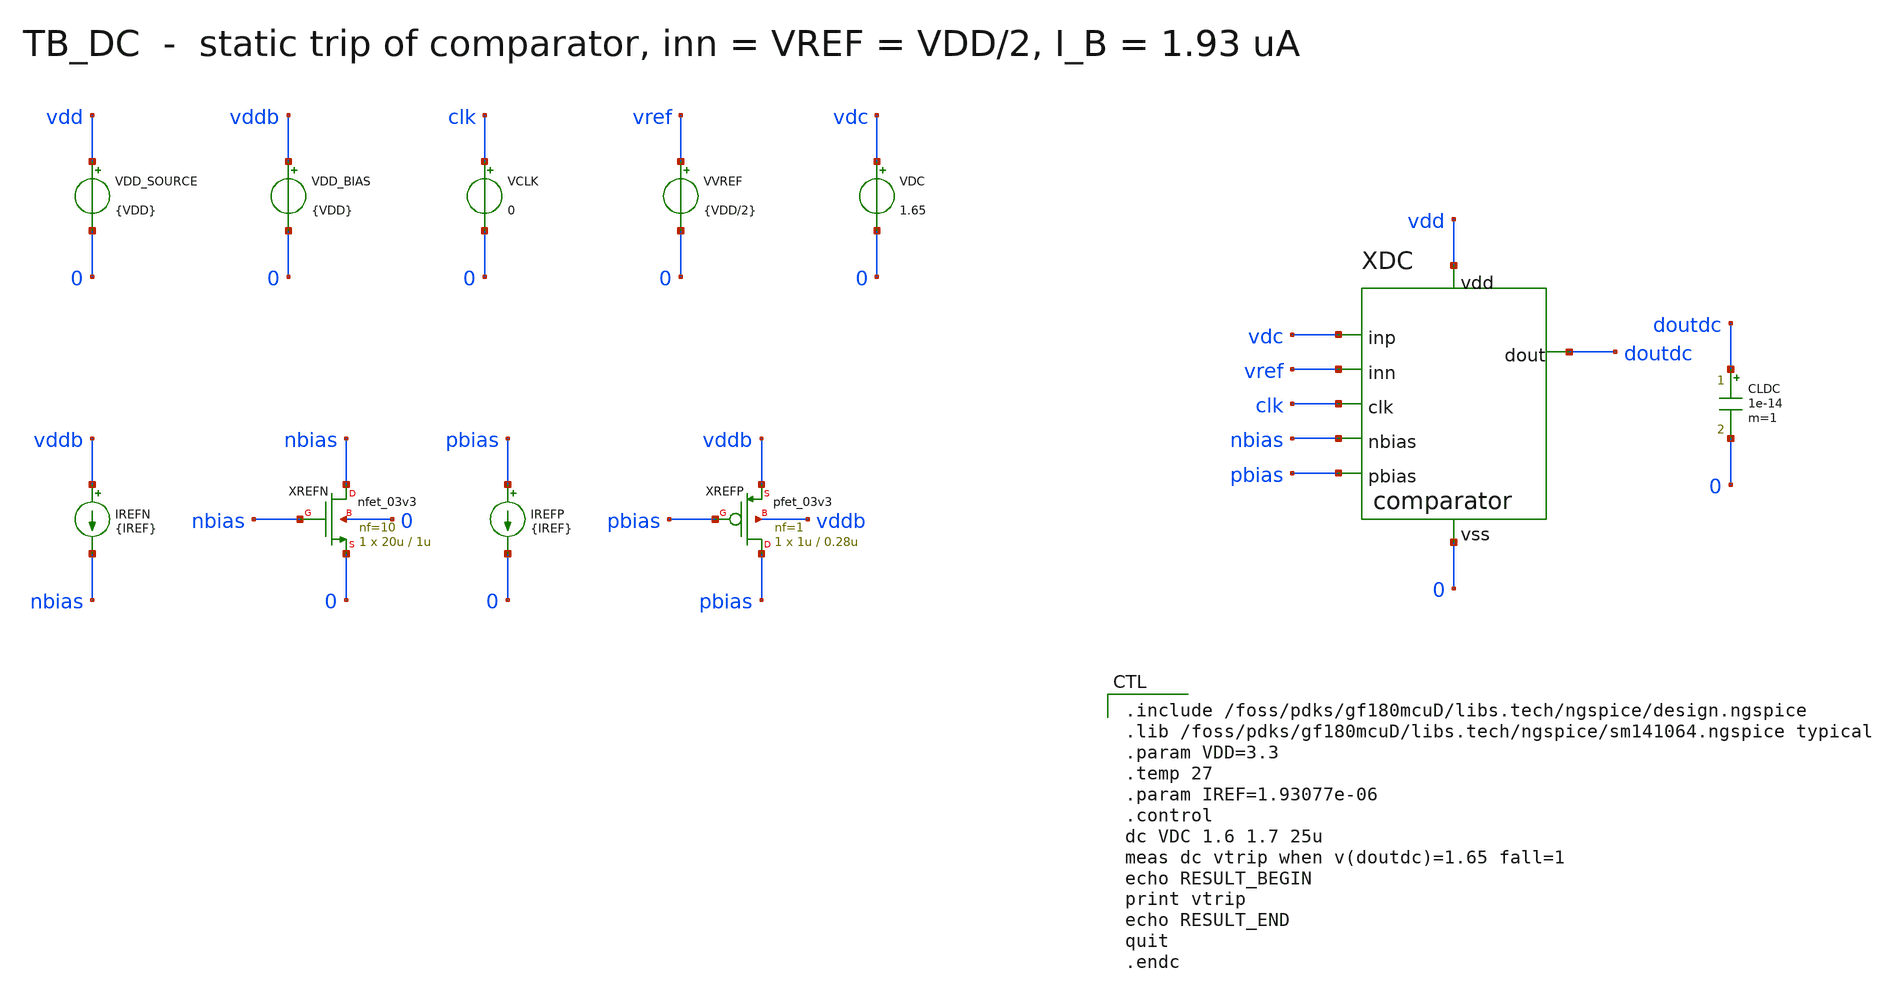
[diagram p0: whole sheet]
** sch_path: mixed_signal/comparator/tb_dc.sch
**.subckt tb_dc
VDD_SOURCE vdd 0 {VDD}
VDD_BIAS vddb 0 {VDD}
IREFN vddb nbias {IREF}
XREFN nbias nbias 0 0 nfet_03v3 L=1u W=20u nf=10 ad='int((nf+1)/2) * W/nf * 0.18u' as='int((nf+2)/2) * W/nf * 0.18u'
+ pd='2*int((nf+1)/2) * (W/nf + 0.18u)' ps='2*int((nf+2)/2) * (W/nf + 0.18u)' nrd='0.18u / W' nrs='0.18u / W'
+ sa=0 sb=0 sd=0 m=1
IREFP pbias 0 {IREF}
XREFP pbias pbias vddb vddb pfet_03v3 L=0.28u W=1u nf=1 ad='int((nf+1)/2) * W/nf * 0.18u' as='int((nf+2)/2) * W/nf * 0.18u'
+ pd='2*int((nf+1)/2) * (W/nf + 0.18u)' ps='2*int((nf+2)/2) * (W/nf + 0.18u)' nrd='0.18u / W' nrs='0.18u / W'
+ sa=0 sb=0 sd=0 m=1
VCLK clk 0 0
VVREF vref 0 {VDD/2}
VDC vdc 0 1.65
XDC vdc vref doutdc clk vdd 0 nbias pbias comparator
CLDC doutdc 0 1e-14 m=1
**** begin user architecture code

.include /foss/pdks/gf180mcuD/libs.tech/ngspice/design.ngspice
.lib /foss/pdks/gf180mcuD/libs.tech/ngspice/sm141064.ngspice typical
.param VDD=3.3
.temp 27
.param IREF=1.93077e-06
.control
dc VDC 1.6 1.7 25u
meas dc vtrip when v(doutdc)=1.65 fall=1
echo RESULT_BEGIN
print vtrip
echo RESULT_END
quit
.endc

**** end user architecture code
**.ends

* expanding   symbol:  comparator.sym # of pins=8
** sym_path: mixed_signal/comparator/comparator.sym
** sch_path: mixed_signal/comparator/comparator.sch
.subckt comparator inp inn dout clk vdd vss nbias pbias
*.iopin vdd
*.iopin vss
*.ipin pbias
*.ipin inp
*.ipin inn
*.opin dout
*.ipin clk
*.ipin nbias
XINP left inp tail vdd pfet_03v3 L=0.32u W=12u nf=12 ad='int((nf+1)/2) * W/nf * 0.18u' as='int((nf+2)/2) * W/nf * 0.18u'
+ pd='2*int((nf+1)/2) * (W/nf + 0.18u)' ps='2*int((nf+2)/2) * (W/nf + 0.18u)' nrd='0.18u / W' nrs='0.18u / W'
+ sa=0 sb=0 sd=0 m=1
XINN outa inn tail vdd pfet_03v3 L=0.32u W=12u nf=12 ad='int((nf+1)/2) * W/nf * 0.18u' as='int((nf+2)/2) * W/nf * 0.18u'
+ pd='2*int((nf+1)/2) * (W/nf + 0.18u)' ps='2*int((nf+2)/2) * (W/nf + 0.18u)' nrd='0.18u / W' nrs='0.18u / W'
+ sa=0 sb=0 sd=0 m=1
XLOADD left left vss vss nfet_03v3 L=0.36u W=0.5u nf=1 ad='int((nf+1)/2) * W/nf * 0.18u' as='int((nf+2)/2) * W/nf * 0.18u'
+ pd='2*int((nf+1)/2) * (W/nf + 0.18u)' ps='2*int((nf+2)/2) * (W/nf + 0.18u)' nrd='0.18u / W' nrs='0.18u / W'
+ sa=0 sb=0 sd=0 m=1
XLOADM outa left vss vss nfet_03v3 L=0.36u W=0.5u nf=1 ad='int((nf+1)/2) * W/nf * 0.18u' as='int((nf+2)/2) * W/nf * 0.18u'
+ pd='2*int((nf+1)/2) * (W/nf + 0.18u)' ps='2*int((nf+2)/2) * (W/nf + 0.18u)' nrd='0.18u / W' nrs='0.18u / W'
+ sa=0 sb=0 sd=0 m=1
XTAIL tail pbias vdd vdd pfet_03v3 L=0.28u W=11u nf=11 ad='int((nf+1)/2) * W/nf * 0.18u' as='int((nf+2)/2) * W/nf * 0.18u'
+ pd='2*int((nf+1)/2) * (W/nf + 0.18u)' ps='2*int((nf+2)/2) * (W/nf + 0.18u)' nrd='0.18u / W' nrs='0.18u / W'
+ sa=0 sb=0 sd=0 m=1
XBST bst pbias vdd vdd pfet_03v3 L=0.28u W=5u nf=5 ad='int((nf+1)/2) * W/nf * 0.18u' as='int((nf+2)/2) * W/nf * 0.18u'
+ pd='2*int((nf+1)/2) * (W/nf + 0.18u)' ps='2*int((nf+2)/2) * (W/nf + 0.18u)' nrd='0.18u / W' nrs='0.18u / W'
+ sa=0 sb=0 sd=0 m=1
XBUF1 outb outa vss vss nfet_03v3 L=0.36u W=0.5u nf=1 ad='int((nf+1)/2) * W/nf * 0.18u' as='int((nf+2)/2) * W/nf * 0.18u'
+ pd='2*int((nf+1)/2) * (W/nf + 0.18u)' ps='2*int((nf+2)/2) * (W/nf + 0.18u)' nrd='0.18u / W' nrs='0.18u / W'
+ sa=0 sb=0 sd=0 m=1
XBUF2 outb outa bst vdd pfet_03v3 L=0.36u W=1u nf=1 ad='int((nf+1)/2) * W/nf * 0.18u' as='int((nf+2)/2) * W/nf * 0.18u'
+ pd='2*int((nf+1)/2) * (W/nf + 0.18u)' ps='2*int((nf+2)/2) * (W/nf + 0.18u)' nrd='0.18u / W' nrs='0.18u / W'
+ sa=0 sb=0 sd=0 m=1
XBUF3 outc outb vss vss nfet_03v3 L=0.36u W=0.5u nf=1 ad='int((nf+1)/2) * W/nf * 0.18u' as='int((nf+2)/2) * W/nf * 0.18u'
+ pd='2*int((nf+1)/2) * (W/nf + 0.18u)' ps='2*int((nf+2)/2) * (W/nf + 0.18u)' nrd='0.18u / W' nrs='0.18u / W'
+ sa=0 sb=0 sd=0 m=1
XBUF4 outc outb vdd vdd pfet_03v3 L=0.36u W=1u nf=1 ad='int((nf+1)/2) * W/nf * 0.18u' as='int((nf+2)/2) * W/nf * 0.18u'
+ pd='2*int((nf+1)/2) * (W/nf + 0.18u)' ps='2*int((nf+2)/2) * (W/nf + 0.18u)' nrd='0.18u / W' nrs='0.18u / W'
+ sa=0 sb=0 sd=0 m=1
XBUF5 dout outc vss vss nfet_03v3 L=0.36u W=0.5u nf=1 ad='int((nf+1)/2) * W/nf * 0.18u' as='int((nf+2)/2) * W/nf * 0.18u'
+ pd='2*int((nf+1)/2) * (W/nf + 0.18u)' ps='2*int((nf+2)/2) * (W/nf + 0.18u)' nrd='0.18u / W' nrs='0.18u / W'
+ sa=0 sb=0 sd=0 m=1
XBUF6 dout outc vdd vdd pfet_03v3 L=0.36u W=1u nf=1 ad='int((nf+1)/2) * W/nf * 0.18u' as='int((nf+2)/2) * W/nf * 0.18u'
+ pd='2*int((nf+1)/2) * (W/nf + 0.18u)' ps='2*int((nf+2)/2) * (W/nf + 0.18u)' nrd='0.18u / W' nrs='0.18u / W'
+ sa=0 sb=0 sd=0 m=1
.ends

.end
